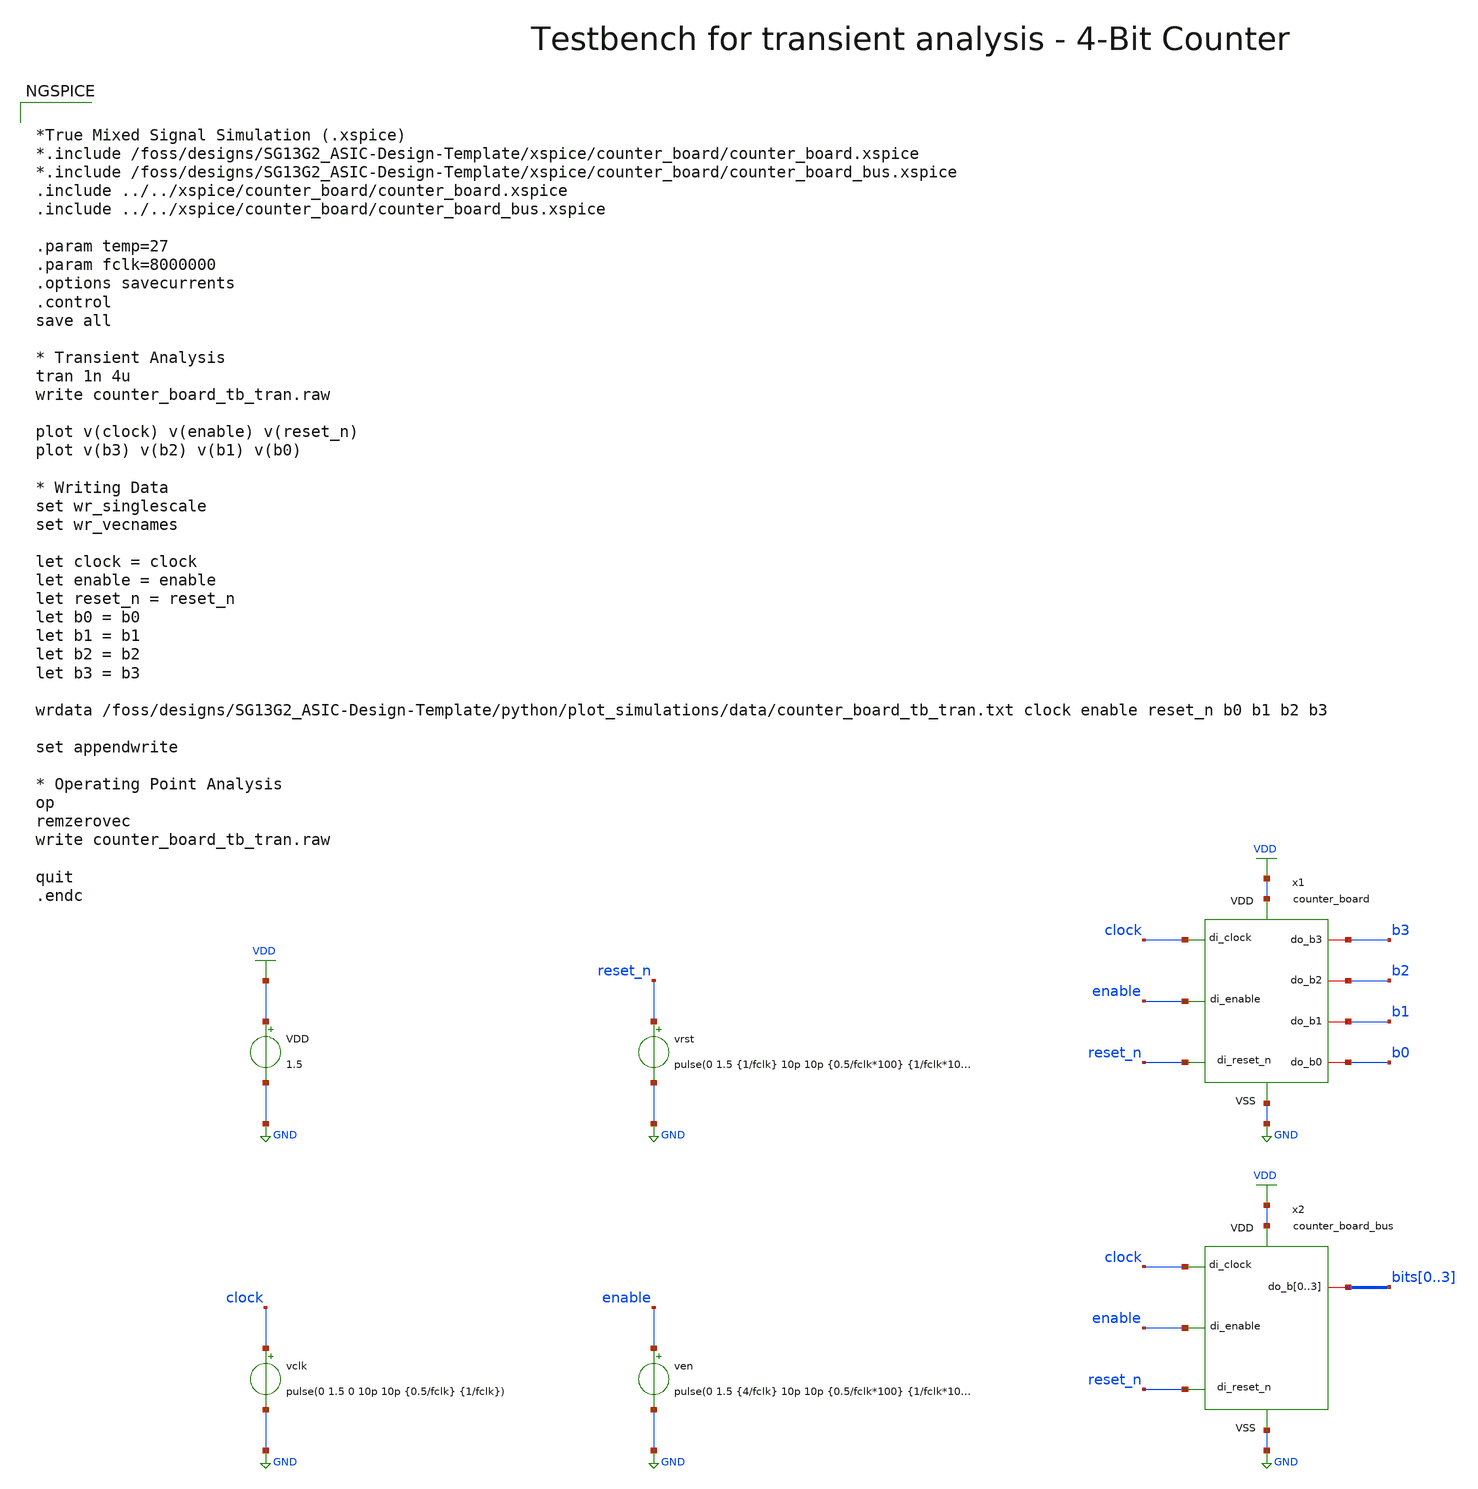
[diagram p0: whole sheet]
** sch_path: xschem/testbenches/counter_board_tb_tran.sch
**.subckt counter_board_tb_tran
VDD VDD GND 1.5
vclk clock GND pulse(0 1.5 0 10p 10p {0.5/fclk} {1/fclk})
vrst reset_n GND pulse(0 1.5 {1/fclk} 10p 10p {0.5/fclk*100} {1/fclk*100})
ven enable GND pulse(0 1.5 {4/fclk} 10p 10p {0.5/fclk*100} {1/fclk*100})
x1 VDD GND clock reset_n enable b0 b1 b2 b3 counter_board
x2 VDD GND clock reset_n enable bits0 bits1 bits2 bits3 counter_board_bus
**** begin user architecture code


*True Mixed Signal Simulation (.xspice)
*.include /foss/designs/SG13G2_ASIC-Design-Template/xspice/counter_board/counter_board.xspice
*.include /foss/designs/SG13G2_ASIC-Design-Template/xspice/counter_board/counter_board_bus.xspice
.include ../../xspice/counter_board/counter_board.xspice
.include ../../xspice/counter_board/counter_board_bus.xspice

.param temp=27
.param fclk=8000000
.options savecurrents
.control
save all

* Transient Analysis
tran 1n 4u
write counter_board_tb_tran.raw

plot v(clock) v(enable) v(reset_n)
plot v(b3) v(b2) v(b1) v(b0)

* Writing Data
set wr_singlescale
set wr_vecnames

let clock = clock
let enable = enable
let reset_n = reset_n
let b0 = b0
let b1 = b1
let b2 = b2
let b3 = b3

wrdata
+ /foss/designs/SG13G2_ASIC-Design-Template/python/plot_simulations/data/counter_board_tb_tran.txt clock enable reset_n b0 b1 b2 b3

set appendwrite

* Operating Point Analysis
op
remzerovec
write counter_board_tb_tran.raw

quit
.endc


.lib cornerMOSlv.lib mos_tt
.lib cornerRES.lib res_typ

**** end user architecture code
**.ends
.GLOBAL GND
.GLOBAL VDD
.end
